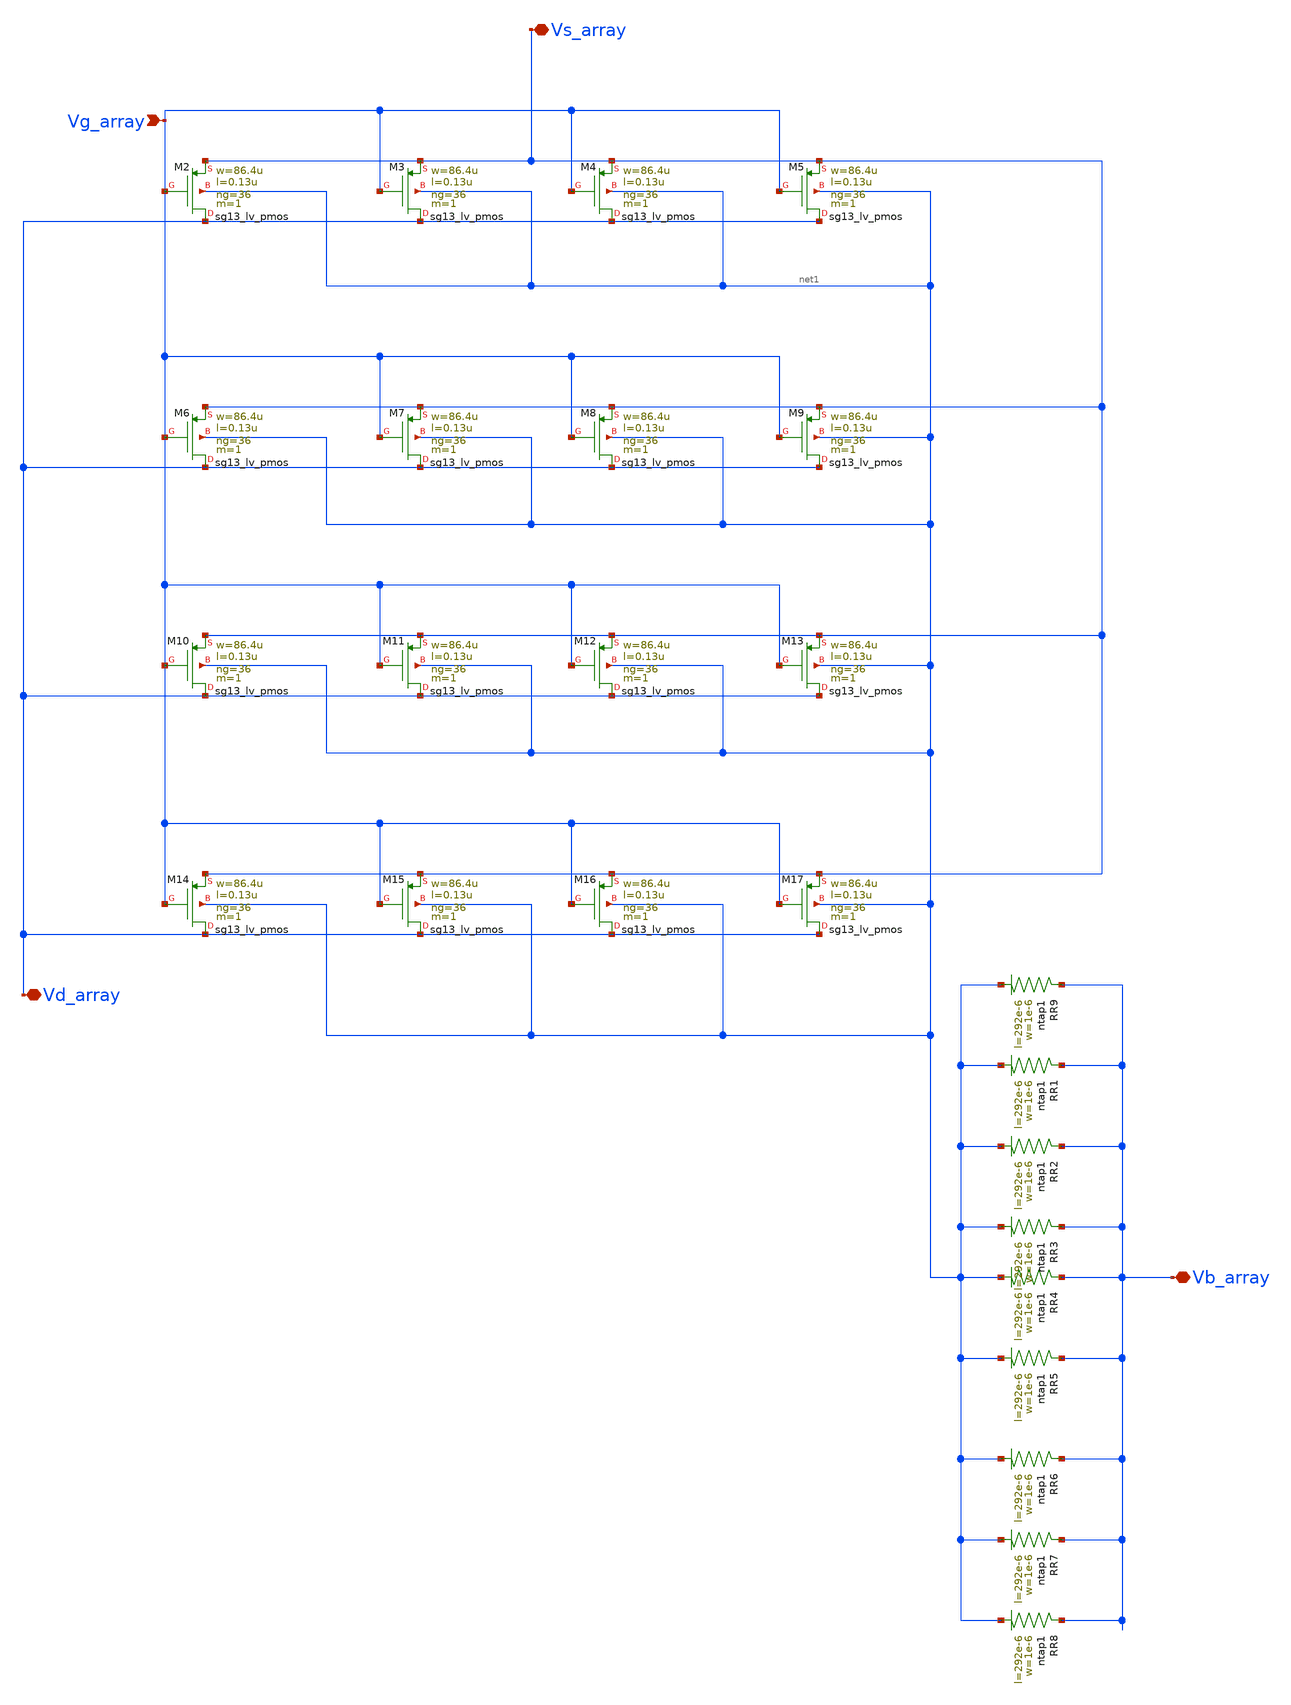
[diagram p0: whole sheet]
** sch_path: Layouts/PMOS/pmos_array.sch
**.subckt pmos_array Vg_array Vs_array Vd_array Vb_array
*.ipin Vg_array
*.iopin Vs_array
*.iopin Vd_array
*.iopin Vb_array
XM2 Vd_array Vg_array Vs_array net1 sg13_lv_pmos w=86.4u l=0.13u ng=36 m=1 mm_ok=1
XM3 Vd_array Vg_array Vs_array net1 sg13_lv_pmos w=86.4u l=0.13u ng=36 m=1 mm_ok=1
XM4 Vd_array Vg_array Vs_array net1 sg13_lv_pmos w=86.4u l=0.13u ng=36 m=1 mm_ok=1
XM5 Vd_array Vg_array Vs_array net1 sg13_lv_pmos w=86.4u l=0.13u ng=36 m=1 mm_ok=1
XM6 Vd_array Vg_array Vs_array net1 sg13_lv_pmos w=86.4u l=0.13u ng=36 m=1 mm_ok=1
XM7 Vd_array Vg_array Vs_array net1 sg13_lv_pmos w=86.4u l=0.13u ng=36 m=1 mm_ok=1
XM8 Vd_array Vg_array Vs_array net1 sg13_lv_pmos w=86.4u l=0.13u ng=36 m=1 mm_ok=1
XM9 Vd_array Vg_array Vs_array net1 sg13_lv_pmos w=86.4u l=0.13u ng=36 m=1 mm_ok=1
XM10 Vd_array Vg_array Vs_array net1 sg13_lv_pmos w=86.4u l=0.13u ng=36 m=1 mm_ok=1
XM11 Vd_array Vg_array Vs_array net1 sg13_lv_pmos w=86.4u l=0.13u ng=36 m=1 mm_ok=1
XM12 Vd_array Vg_array Vs_array net1 sg13_lv_pmos w=86.4u l=0.13u ng=36 m=1 mm_ok=1
XM13 Vd_array Vg_array Vs_array net1 sg13_lv_pmos w=86.4u l=0.13u ng=36 m=1 mm_ok=1
XM14 Vd_array Vg_array Vs_array net1 sg13_lv_pmos w=86.4u l=0.13u ng=36 m=1 mm_ok=1
XM15 Vd_array Vg_array Vs_array net1 sg13_lv_pmos w=86.4u l=0.13u ng=36 m=1 mm_ok=1
XM16 Vd_array Vg_array Vs_array net1 sg13_lv_pmos w=86.4u l=0.13u ng=36 m=1 mm_ok=1
XM17 Vd_array Vg_array Vs_array net1 sg13_lv_pmos w=86.4u l=0.13u ng=36 m=1 mm_ok=1
XR9 Vb_array net1 ntap1 R=1.116 w=1e-6 l=292e-6
XR1 Vb_array net1 ntap1 R=1.116 w=1e-6 l=292e-6
XR2 Vb_array net1 ntap1 R=1.116 w=1e-6 l=292e-6
XR3 Vb_array net1 ntap1 R=1.116 w=1e-6 l=292e-6
XR4 Vb_array net1 ntap1 R=1.116 w=1e-6 l=292e-6
XR5 Vb_array net1 ntap1 R=1.116 w=1e-6 l=292e-6
XR6 Vb_array net1 ntap1 R=1.116 w=1e-6 l=292e-6
XR7 Vb_array net1 ntap1 R=1.116 w=1e-6 l=292e-6
XR8 Vb_array net1 ntap1 R=1.116 w=1e-6 l=292e-6
**.ends
.end
